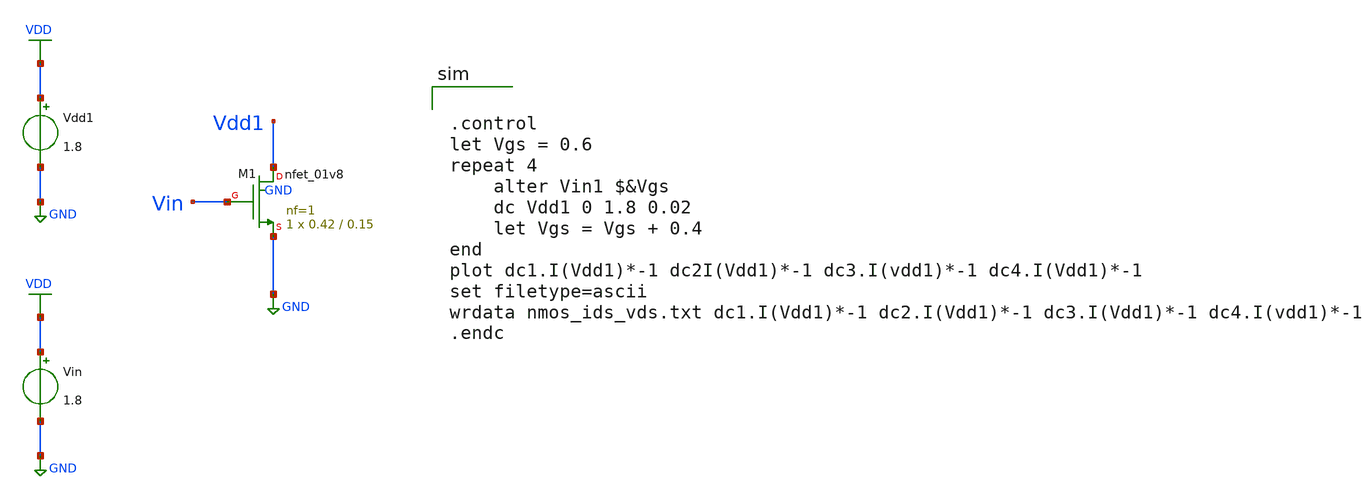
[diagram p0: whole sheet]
** sch_path: tutorials/tutorial_1/tutorial1b.sch
**.subckt tutorial1b
Vdd1 VDD GND 1.8
Vin VDD GND 1.8
XM1 Vdd1 Vin GND GND sky130_fd_pr__nfet_01v8 L=0.15 W=0.42 nf=1 ad='int((1 + 1)/2) * 0.42 / 1 * 0.29'
+ as='int((1 + 2)/2) * 0.42 / 1 * 0.29' pd='2*int((1 + 1)/2) * (0.42 / 1 + 0.29)' ps='2*int((1 + 2)/2) * (0.42 / 1 + 0.29)'
+ nrd='0.29 / 0.42 ' nrs='0.29 / 0.42 ' sa=0 sb=0 sd=0 mult=1 m=1
**** begin user architecture code


.control
let Vgs = 0.6
repeat 4
	alter Vin1 $&Vgs
	dc Vdd1 0 1.8 0.02
	let Vgs = Vgs + 0.4
end
plot dc1.I(Vdd1)*-1 dc2I(Vdd1)*-1 dc3.I(vdd1)*-1 dc4.I(Vdd1)*-1
set filetype=ascii
wrdata nmos_ids_vds.txt dc1.I(Vdd1)*-1 dc2.I(Vdd1)*-1 dc3.I(Vdd1)*-1 dc4.I(vdd1)*-1
.endc


**** end user architecture code
**.ends
.GLOBAL GND
.GLOBAL VDD
.end
